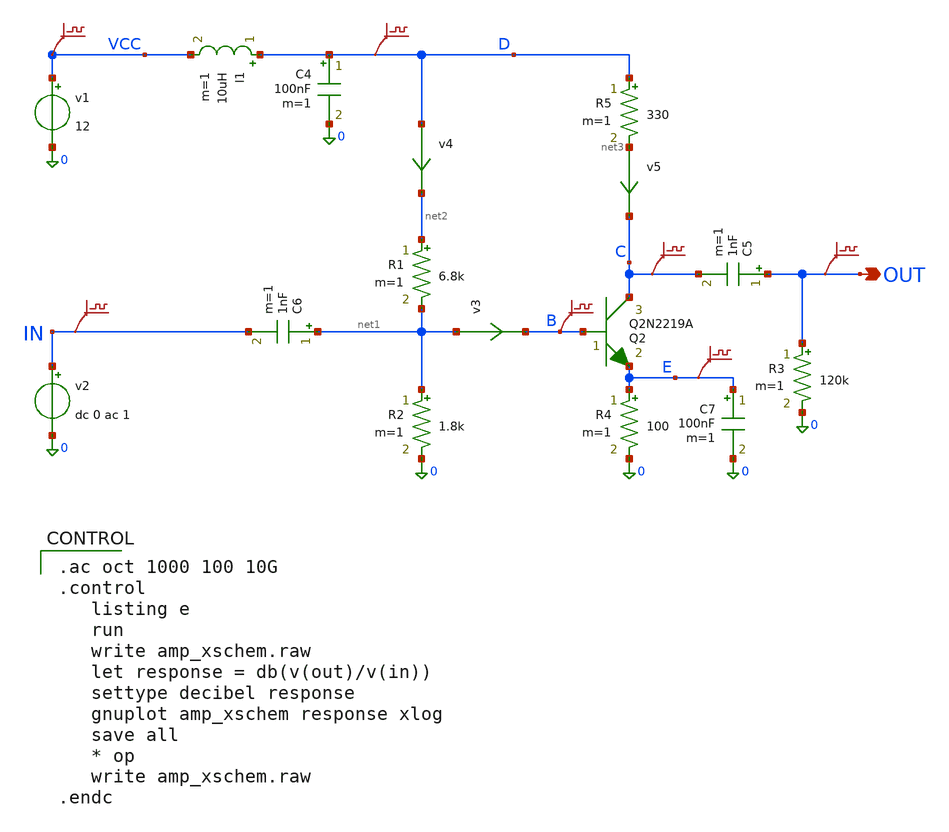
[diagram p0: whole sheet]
** sch_path: xschem_libraries_oa/ngspice/amp_xschem/schematic/amp_xschem.sch
* Copyright (C) 1998-2024 Stefan Frederik Schippers
* This program is free software; you can redistribute it and/or modify
* it under the terms of the GNU General Public License as published by
* the Free Software Foundation; either version 2 of the License, or
* (at your option) any later version.
* This program is distributed in the hope that it will be useful,
* but WITHOUT ANY WARRANTY; without even the implied warranty of
* MERCHANTABILITY or FITNESS FOR A PARTICULAR PURPOSE.  See the
* GNU General Public License for more details.
* You should have received a copy of the GNU General Public License
* along with this program; if not, write to the Free Software
**.subckt amp_xschem OUT
*.opin OUT
l1 D VCC 10uH m=1
v1 VCC 0 12
C4 D 0 100nF m=1
R1 net2 net1 6.8k m=1
Q2 C B E Q2N2219A area=1 m=1
R2 net1 0 1.8k m=1
C5 OUT C 1nF m=1
R3 OUT 0 120k m=1
R4 E 0 100 m=1
C6 net1 IN 1nF m=1
v2 IN 0 dc 0 ac 1
R5 D net3 330 m=1
C7 E 0 100nF m=1
v3 net1 B 0
.save i(v3)
v4 D net2 0
.save i(v4)
v5 net3 C 0
.save i(v5)
.save v(out)
.save v(c)
.save v(vcc)
.save v(in)
.save v(b)
.save v(e)
.save v(d)
**** begin user architecture code

.model Q2N2219A  NPN(Is=14.34f Xti=3 Eg=1.11 Vaf=74.03 Bf=255.9 Ne=1.307 Ise=14.34f Ikf=.2847
+ Xtb=1.5 Br=6.092 Nc=2 Isc=0 Ikr=0 Rc=1 Cjc=7.306p  Mjc=.3416 Vjc=.75 Fc=.5 Cje=22.01p Mje=.377 Vje=.75
+ Tr=46.91n Tf=411.1p Itf=.6 Vtf=1.7 Xtf=3 Rb=10 Vceo=40 Icrating=800m )


**** end user architecture code
**.ends
**** begin user architecture code

.ac oct 1000 100 10G
.control
   listing e
   run
   write amp_xschem.raw
   let response = db(v(out)/v(in))
   settype decibel response
   gnuplot amp_xschem response xlog
   save all
   * op
   write amp_xschem.raw
.endc



**** end user architecture code
.end
